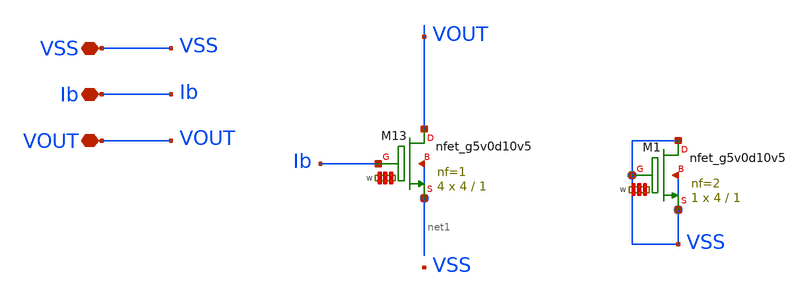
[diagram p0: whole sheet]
** sch_path: Learning/single_ended_amplifiers/Design_and_Analysis_of_Two-Stage_CMOS_Operational_Amplifier_for_Fluorescence_Signal_Processing_sky130_5V/layout_magic/input_second_stage.sch
**.subckt input_second_stage VSS Ib VOUT
*.iopin VSS
*.iopin Ib
*.iopin VOUT
XM13 VOUT Ib net1 net1 sky130_fd_pr__nfet_g5v0d10v5 L=1 W='4 * 1 ' nf=1 ad='int((nf+1)/2) * W / nf * 0.29'
+ as='int((nf+2)/2) * W / nf * 0.29' pd='2*int((nf+1)/2) * (W / nf + 0.29)' ps='2*int((nf+2)/2) * (W / nf + 0.29)'
+ nrd='0.29 / W ' nrs='0.29 / W ' sa=0 sb=0 sd=0 mult=4 m=4
XM1 VSS VSS VSS VSS sky130_fd_pr__nfet_g5v0d10v5 L=1 W='4 * 2 ' nf=2 ad='int((nf+1)/2) * W / nf * 0.29'
+ as='int((nf+2)/2) * W / nf * 0.29' pd='2*int((nf+1)/2) * (W / nf + 0.29)' ps='2*int((nf+2)/2) * (W / nf + 0.29)'
+ nrd='0.29 / W ' nrs='0.29 / W ' sa=0 sb=0 sd=0 mult=1 m=1
**.ends
.end
